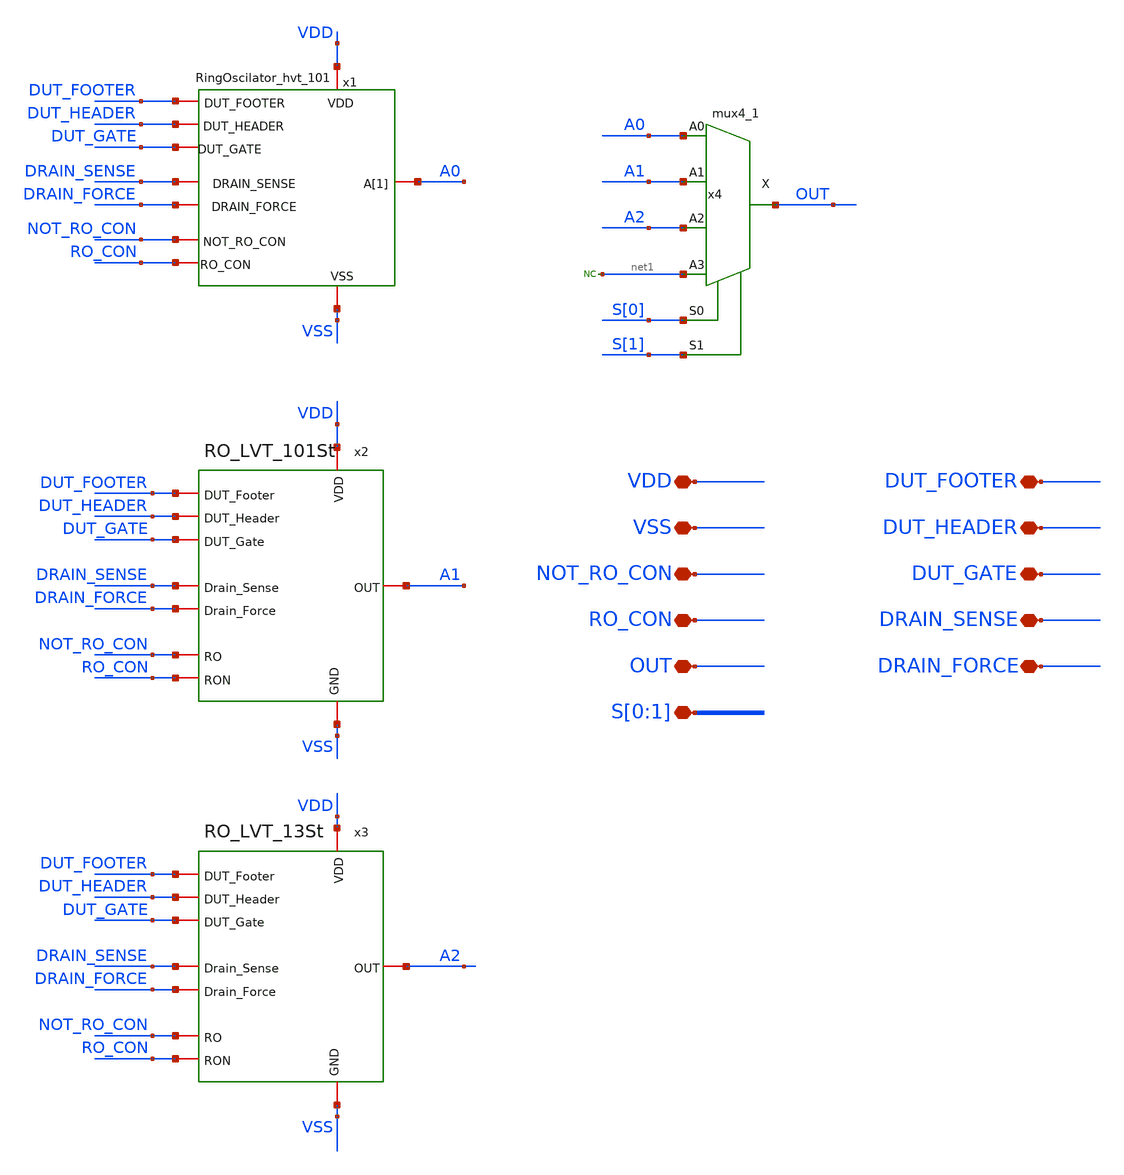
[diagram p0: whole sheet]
** sch_path: TOP/TOP.sch
**.subckt TOP VDD VSS NOT_RO_CON RO_CON DUT_FOOTER DUT_HEADER DUT_GATE DRAIN_SENSE DRAIN_FORCE OUT
*+ S[0],S[1]
*.iopin VDD
*.iopin VSS
*.iopin NOT_RO_CON
*.iopin RO_CON
*.iopin DUT_FOOTER
*.iopin DUT_HEADER
*.iopin DUT_GATE
*.iopin DRAIN_SENSE
*.iopin DRAIN_FORCE
*.iopin OUT
*.iopin S[0],S[1]
x1 DUT_FOOTER VDD DUT_HEADER VSS DUT_GATE NOT_RO_CON RO_CON DRAIN_SENSE A0 DRAIN_FORCE
+ RingOscilator_hvt_101
x2 VDD VSS DUT_FOOTER DUT_HEADER DRAIN_SENSE DRAIN_FORCE NOT_RO_CON RO_CON DUT_GATE A1 RO_LVT_101St
x3 VDD VSS DUT_FOOTER DUT_HEADER DRAIN_SENSE DRAIN_FORCE NOT_RO_CON RO_CON DUT_GATE A2 RO_LVT_13St
x4 A0 A1 A2 net1 S[0] S[1] VGND VNB VPB VPWR OUT sky130_fd_sc_hd__mux4_1
* noconn #net1
**.ends
.end
